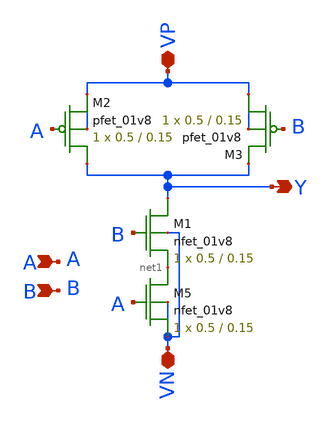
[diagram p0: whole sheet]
** sch_path: lib/digital/schematic/nand.sch
**.subckt nand B VP VN A Y
*.ipin B
*.iopin VP
*.iopin VN
*.ipin A
*.opin Y
XM1 Y B net1 VN sky130_fd_pr__nfet_01v8 L=0.15 W=0.5 nf=1 ad='int((nf+1)/2) * W/nf * 0.29' as='int((nf+2)/2) * W/nf * 0.29'
+ pd='2*int((nf+1)/2) * (W/nf + 0.29)' ps='2*int((nf+2)/2) * (W/nf + 0.29)' nrd='0.29 / W' nrs='0.29 / W'
+ sa=0 sb=0 sd=0 mult=1 m=1
XM2 Y A VP VP sky130_fd_pr__pfet_01v8 L=0.15 W=0.5 nf=1 ad='int((nf+1)/2) * W/nf * 0.29' as='int((nf+2)/2) * W/nf * 0.29'
+ pd='2*int((nf+1)/2) * (W/nf + 0.29)' ps='2*int((nf+2)/2) * (W/nf + 0.29)' nrd='0.29 / W' nrs='0.29 / W'
+ sa=0 sb=0 sd=0 mult=1 m=1
XM3 VP B Y VP sky130_fd_pr__pfet_01v8 L=0.15 W=0.5 nf=1 ad='int((nf+1)/2) * W/nf * 0.29' as='int((nf+2)/2) * W/nf * 0.29'
+ pd='2*int((nf+1)/2) * (W/nf + 0.29)' ps='2*int((nf+2)/2) * (W/nf + 0.29)' nrd='0.29 / W' nrs='0.29 / W'
+ sa=0 sb=0 sd=0 mult=1 m=1
XM5 net1 A VN VN sky130_fd_pr__nfet_01v8 L=0.15 W=0.5 nf=1 ad='int((nf+1)/2) * W/nf * 0.29' as='int((nf+2)/2) * W/nf * 0.29'
+ pd='2*int((nf+1)/2) * (W/nf + 0.29)' ps='2*int((nf+2)/2) * (W/nf + 0.29)' nrd='0.29 / W' nrs='0.29 / W'
+ sa=0 sb=0 sd=0 mult=1 m=1
**.ends
.end
